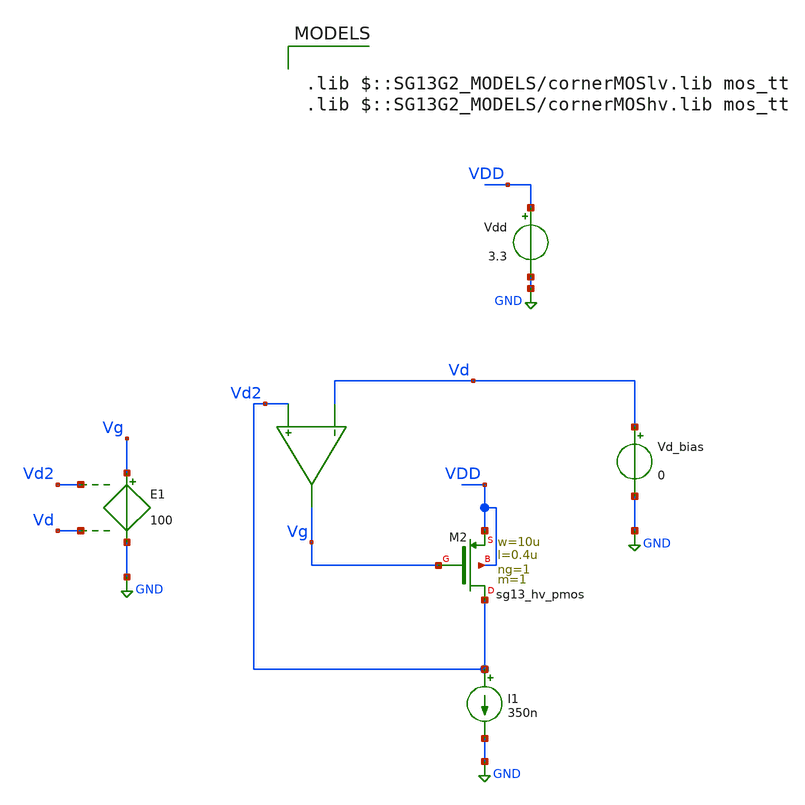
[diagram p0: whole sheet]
** sch_path: legacy/Examples/IHP-SG13/xschem/Extraction/pmos_sigma_ext.sch
**.subckt pmos_sigma_ext
I1 Vd2 GND 350n
Vd_bias Vd GND 0
Vdd VDD GND 3.3
E1 Vg GND Vd2 Vd 100
XM2 Vd2 Vg VDD VDD sg13_hv_pmos w=10u l=0.4u ng=1 m=1 mm_ok=1
**** begin user architecture code



.control
pre_osdi ./psp103_nqs.osdi
save all

dc Vd_bias  0 -4 -25.9m

let vd_interp = -3.3/3
let sigma = -deriv(V(vg))/deriv(V(vd))
save sigma

echo
echo
echo


echo Sigma @ VD=$&vd_interp:
meas dc sigma_value FIND sigma WHEN V(vd)=vd_interp

echo
echo
echo
write pmos_sigma_ext.raw

.endc





.lib $::SG13G2_MODELS/cornerMOSlv.lib mos_tt
.lib $::SG13G2_MODELS/cornerMOShv.lib mos_tt

**** end user architecture code
**.ends
.GLOBAL GND
.end
